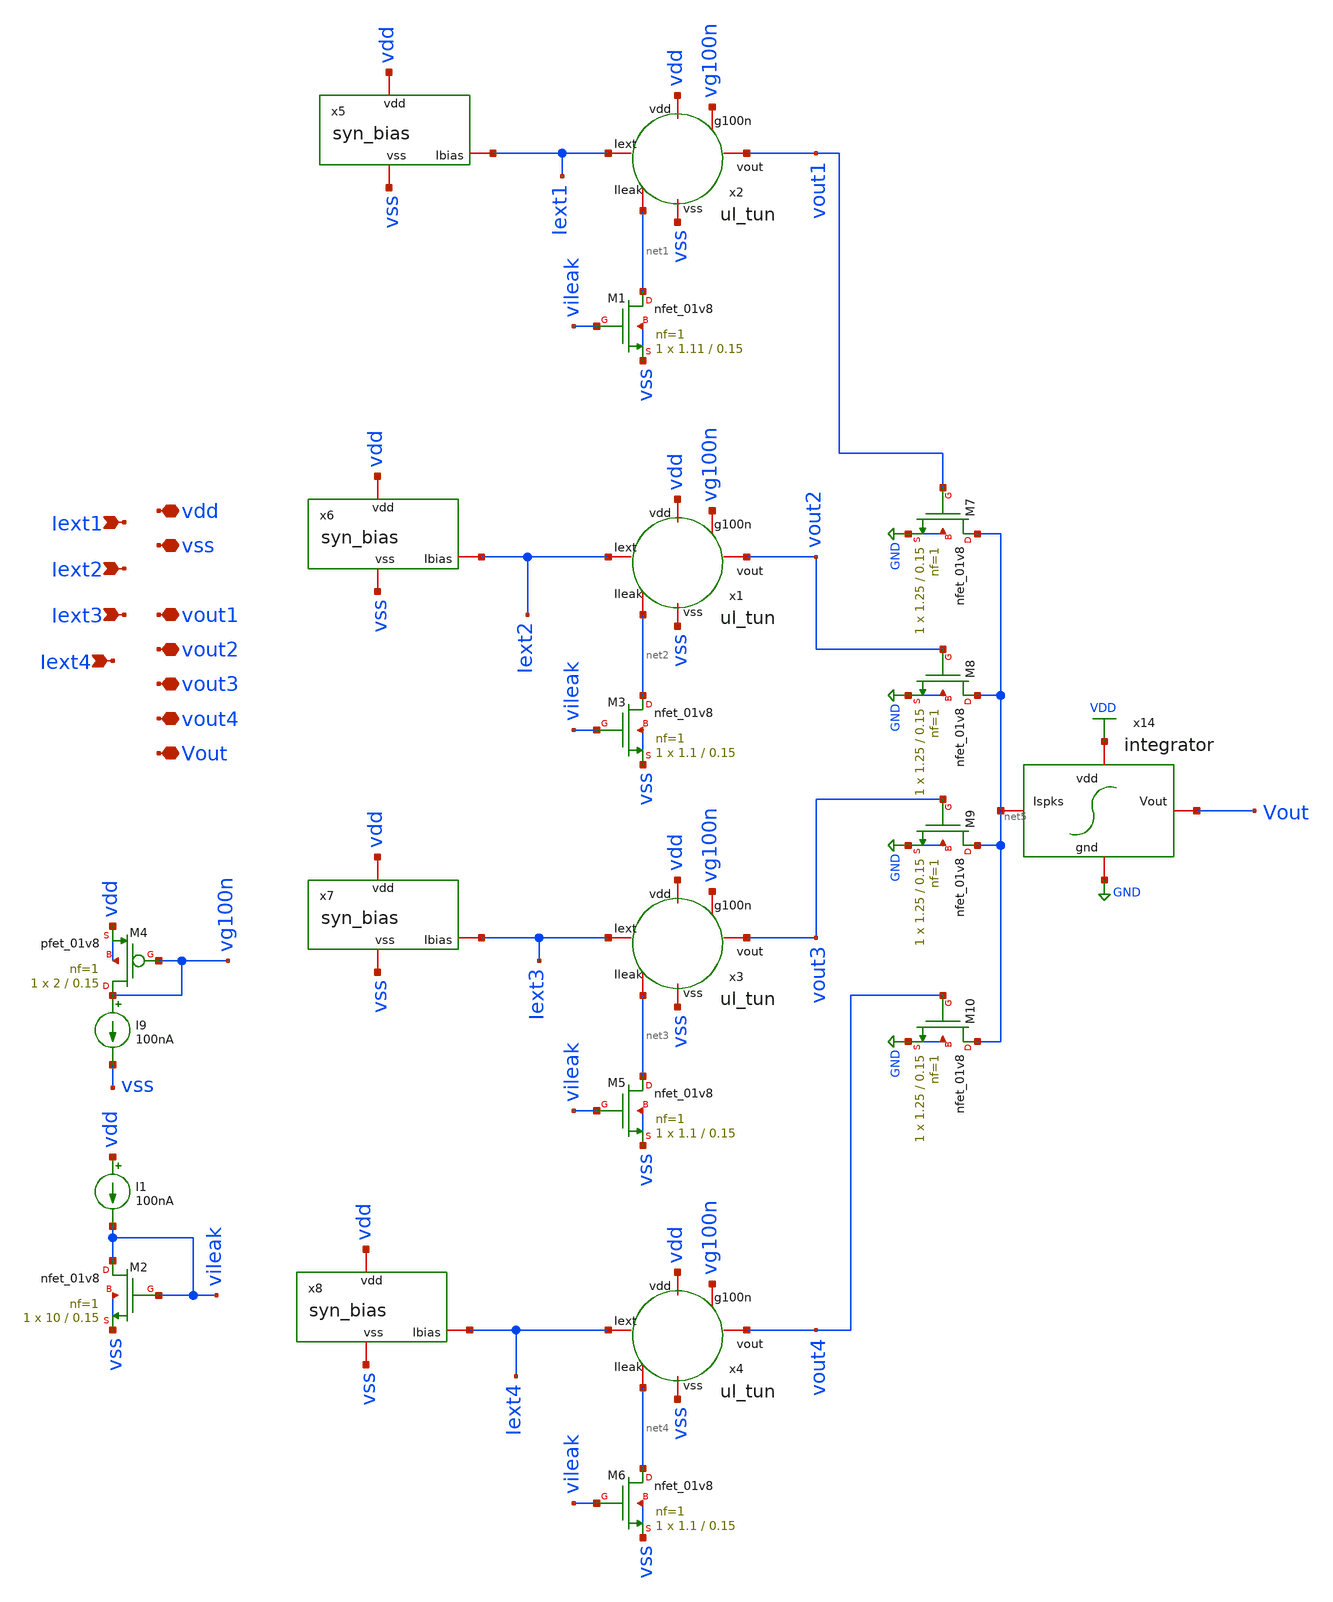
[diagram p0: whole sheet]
** sch_path: layer/layer_output.sch
**.subckt layer_output vdd vss Iext1 Vout Iext2 Iext3 Iext4 vout1 vout2 vout3 vout4
*.iopin vdd
*.iopin vss
*.ipin Iext1
*.iopin Vout
*.ipin Iext2
*.ipin Iext3
*.ipin Iext4
*.iopin vout1
*.iopin vout2
*.iopin vout3
*.iopin vout4
x2 Iext1 vdd vg100n vout1 net1 vss ul_tun
I9 vg100n vss 100nA
XM4 vg100n vg100n vdd vdd sky130_fd_pr__pfet_01v8 L=0.15 W=2 nf=1 ad='int((nf+1)/2) * W/nf * 0.29' as='int((nf+2)/2) * W/nf * 0.29'
+ pd='2*int((nf+1)/2) * (W/nf + 0.29)' ps='2*int((nf+2)/2) * (W/nf + 0.29)' nrd='0.29 / W' nrs='0.29 / W'
+ sa=0 sb=0 sd=0 mult=1 m=1
XM1 net1 vileak vss vss sky130_fd_pr__nfet_01v8 L=0.15 W=1.11 nf=1 ad='int((nf+1)/2) * W/nf * 0.29' as='int((nf+2)/2) * W/nf * 0.29'
+ pd='2*int((nf+1)/2) * (W/nf + 0.29)' ps='2*int((nf+2)/2) * (W/nf + 0.29)' nrd='0.29 / W' nrs='0.29 / W'
+ sa=0 sb=0 sd=0 mult=1 m=1
XM2 vileak vileak vss vss sky130_fd_pr__nfet_01v8 L=0.15 W=10 nf=1 ad='int((nf+1)/2) * W/nf * 0.29' as='int((nf+2)/2) * W/nf * 0.29'
+ pd='2*int((nf+1)/2) * (W/nf + 0.29)' ps='2*int((nf+2)/2) * (W/nf + 0.29)' nrd='0.29 / W' nrs='0.29 / W'
+ sa=0 sb=0 sd=0 mult=1 m=1
I1 vdd vileak 100nA
x1 Iext2 vdd vg100n vout2 net2 vss ul_tun
XM3 net2 vileak vss vss sky130_fd_pr__nfet_01v8 L=0.15 W=1.1 nf=1 ad='int((nf+1)/2) * W/nf * 0.29' as='int((nf+2)/2) * W/nf * 0.29'
+ pd='2*int((nf+1)/2) * (W/nf + 0.29)' ps='2*int((nf+2)/2) * (W/nf + 0.29)' nrd='0.29 / W' nrs='0.29 / W'
+ sa=0 sb=0 sd=0 mult=1 m=1
x3 Iext3 vdd vg100n vout3 net3 vss ul_tun
XM5 net3 vileak vss vss sky130_fd_pr__nfet_01v8 L=0.15 W=1.1 nf=1 ad='int((nf+1)/2) * W/nf * 0.29' as='int((nf+2)/2) * W/nf * 0.29'
+ pd='2*int((nf+1)/2) * (W/nf + 0.29)' ps='2*int((nf+2)/2) * (W/nf + 0.29)' nrd='0.29 / W' nrs='0.29 / W'
+ sa=0 sb=0 sd=0 mult=1 m=1
x4 Iext4 vdd vg100n vout4 net4 vss ul_tun
XM6 net4 vileak vss vss sky130_fd_pr__nfet_01v8 L=0.15 W=1.1 nf=1 ad='int((nf+1)/2) * W/nf * 0.29' as='int((nf+2)/2) * W/nf * 0.29'
+ pd='2*int((nf+1)/2) * (W/nf + 0.29)' ps='2*int((nf+2)/2) * (W/nf + 0.29)' nrd='0.29 / W' nrs='0.29 / W'
+ sa=0 sb=0 sd=0 mult=1 m=1
x14 VDD Vout net5 GND integrator
XM7 net5 vout1 GND GND sky130_fd_pr__nfet_01v8 L=0.15 W=1.25 nf=1 ad='int((nf+1)/2) * W/nf * 0.29' as='int((nf+2)/2) * W/nf * 0.29'
+ pd='2*int((nf+1)/2) * (W/nf + 0.29)' ps='2*int((nf+2)/2) * (W/nf + 0.29)' nrd='0.29 / W' nrs='0.29 / W'
+ sa=0 sb=0 sd=0 mult=1 m=1
XM8 net5 vout2 GND GND sky130_fd_pr__nfet_01v8 L=0.15 W=1.25 nf=1 ad='int((nf+1)/2) * W/nf * 0.29' as='int((nf+2)/2) * W/nf * 0.29'
+ pd='2*int((nf+1)/2) * (W/nf + 0.29)' ps='2*int((nf+2)/2) * (W/nf + 0.29)' nrd='0.29 / W' nrs='0.29 / W'
+ sa=0 sb=0 sd=0 mult=1 m=1
XM9 net5 vout3 GND GND sky130_fd_pr__nfet_01v8 L=0.15 W=1.25 nf=1 ad='int((nf+1)/2) * W/nf * 0.29' as='int((nf+2)/2) * W/nf * 0.29'
+ pd='2*int((nf+1)/2) * (W/nf + 0.29)' ps='2*int((nf+2)/2) * (W/nf + 0.29)' nrd='0.29 / W' nrs='0.29 / W'
+ sa=0 sb=0 sd=0 mult=1 m=1
XM10 net5 vout4 GND GND sky130_fd_pr__nfet_01v8 L=0.15 W=1.25 nf=1 ad='int((nf+1)/2) * W/nf * 0.29' as='int((nf+2)/2) * W/nf * 0.29'
+ pd='2*int((nf+1)/2) * (W/nf + 0.29)' ps='2*int((nf+2)/2) * (W/nf + 0.29)' nrd='0.29 / W' nrs='0.29 / W'
+ sa=0 sb=0 sd=0 mult=1 m=1
x5 vdd vss Iext1 syn_bias
x6 vdd vss Iext2 syn_bias
x7 vdd vss Iext3 syn_bias
x8 vdd vss Iext4 syn_bias
**.ends
.GLOBAL GND
.GLOBAL VDD
.end
